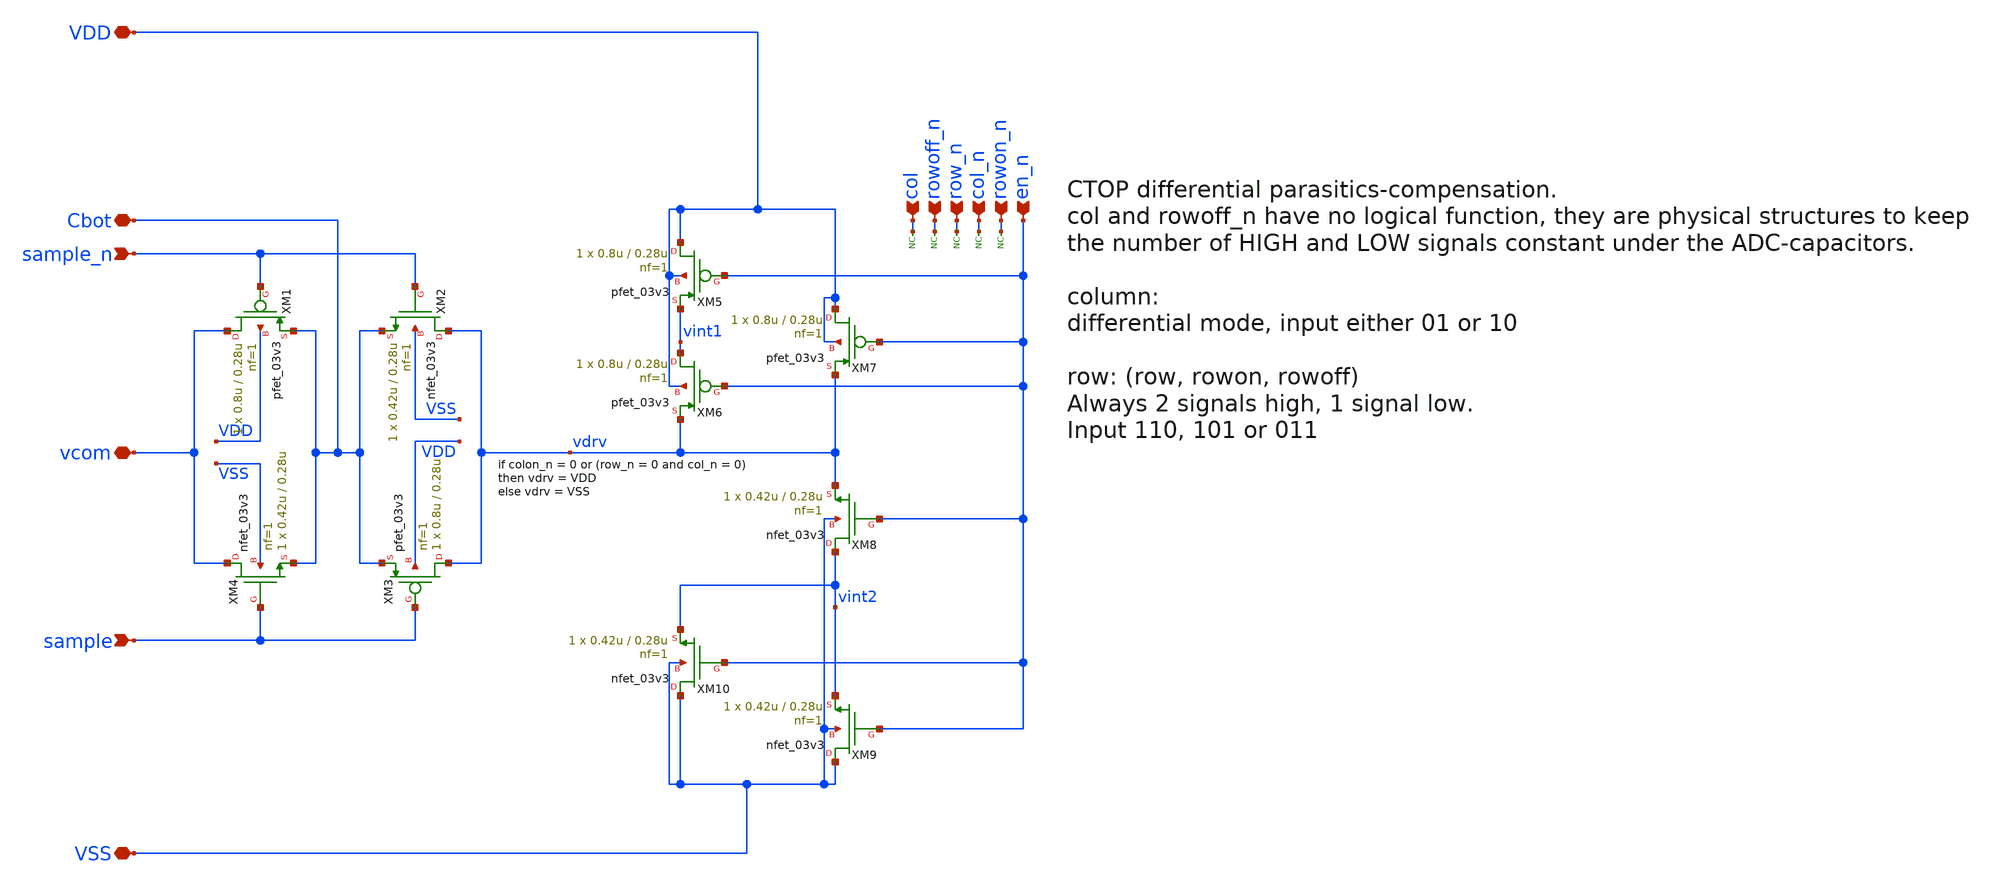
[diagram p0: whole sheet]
** sch_path: adc_sar_array_circuit_2.sch
**.subckt adc_sar_array_circuit_2 sample_n sample vcom row_n col_n rowon_n VDD VSS Cbot en_n
*+ rowoff_n col
*.ipin sample_n
*.ipin sample
*.iopin vcom
*.ipin row_n
*.ipin col_n
*.ipin rowon_n
*.iopin VDD
*.iopin VSS
*.iopin Cbot
*.ipin en_n
*.ipin rowoff_n
*.ipin col
* noconn row_n
* noconn col_n
* noconn rowon_n
* noconn rowoff_n
* noconn col
XM1 vcom sample_n Cbot VDD pfet_03v3 L=0.28u W=0.8u nf=1 ad='int((nf+1)/2) * W/nf * 0.18u' as='int((nf+2)/2) * W/nf * 0.18u'
+ pd='2*int((nf+1)/2) * (W/nf + 0.18u)' ps='2*int((nf+2)/2) * (W/nf + 0.18u)' nrd='0.18u / W' nrs='0.18u / W'
+ sa=0 sb=0 sd=0 m=1
XM2 vdrv sample_n Cbot VSS nfet_03v3 L=0.28u W=0.42u nf=1 ad='int((nf+1)/2) * W/nf * 0.18u' as='int((nf+2)/2) * W/nf * 0.18u'
+ pd='2*int((nf+1)/2) * (W/nf + 0.18u)' ps='2*int((nf+2)/2) * (W/nf + 0.18u)' nrd='0.18u / W' nrs='0.18u / W'
+ sa=0 sb=0 sd=0 m=1
XM3 vdrv sample Cbot VDD pfet_03v3 L=0.28u W=0.8u nf=1 ad='int((nf+1)/2) * W/nf * 0.18u' as='int((nf+2)/2) * W/nf * 0.18u'
+ pd='2*int((nf+1)/2) * (W/nf + 0.18u)' ps='2*int((nf+2)/2) * (W/nf + 0.18u)' nrd='0.18u / W' nrs='0.18u / W'
+ sa=0 sb=0 sd=0 m=1
XM4 vcom sample Cbot VSS nfet_03v3 L=0.28u W=0.42u nf=1 ad='int((nf+1)/2) * W/nf * 0.18u' as='int((nf+2)/2) * W/nf * 0.18u'
+ pd='2*int((nf+1)/2) * (W/nf + 0.18u)' ps='2*int((nf+2)/2) * (W/nf + 0.18u)' nrd='0.18u / W' nrs='0.18u / W'
+ sa=0 sb=0 sd=0 m=1
XM5 VDD en_n vint1 VDD pfet_03v3 L=0.28u W=0.8u nf=1 ad='int((nf+1)/2) * W/nf * 0.18u' as='int((nf+2)/2) * W/nf * 0.18u'
+ pd='2*int((nf+1)/2) * (W/nf + 0.18u)' ps='2*int((nf+2)/2) * (W/nf + 0.18u)' nrd='0.18u / W' nrs='0.18u / W'
+ sa=0 sb=0 sd=0 m=1
XM6 vint1 en_n vdrv VDD pfet_03v3 L=0.28u W=0.8u nf=1 ad='int((nf+1)/2) * W/nf * 0.18u' as='int((nf+2)/2) * W/nf * 0.18u'
+ pd='2*int((nf+1)/2) * (W/nf + 0.18u)' ps='2*int((nf+2)/2) * (W/nf + 0.18u)' nrd='0.18u / W' nrs='0.18u / W'
+ sa=0 sb=0 sd=0 m=1
XM7 VDD en_n vdrv VDD pfet_03v3 L=0.28u W=0.8u nf=1 ad='int((nf+1)/2) * W/nf * 0.18u' as='int((nf+2)/2) * W/nf * 0.18u'
+ pd='2*int((nf+1)/2) * (W/nf + 0.18u)' ps='2*int((nf+2)/2) * (W/nf + 0.18u)' nrd='0.18u / W' nrs='0.18u / W'
+ sa=0 sb=0 sd=0 m=1
XM8 vint2 en_n vdrv VSS nfet_03v3 L=0.28u W=0.42u nf=1 ad='int((nf+1)/2) * W/nf * 0.18u' as='int((nf+2)/2) * W/nf * 0.18u'
+ pd='2*int((nf+1)/2) * (W/nf + 0.18u)' ps='2*int((nf+2)/2) * (W/nf + 0.18u)' nrd='0.18u / W' nrs='0.18u / W'
+ sa=0 sb=0 sd=0 m=1
XM9 VSS en_n vint2 VSS nfet_03v3 L=0.28u W=0.42u nf=1 ad='int((nf+1)/2) * W/nf * 0.18u' as='int((nf+2)/2) * W/nf * 0.18u'
+ pd='2*int((nf+1)/2) * (W/nf + 0.18u)' ps='2*int((nf+2)/2) * (W/nf + 0.18u)' nrd='0.18u / W' nrs='0.18u / W'
+ sa=0 sb=0 sd=0 m=1
XM10 VSS en_n vint2 VSS nfet_03v3 L=0.28u W=0.42u nf=1 ad='int((nf+1)/2) * W/nf * 0.18u' as='int((nf+2)/2) * W/nf * 0.18u'
+ pd='2*int((nf+1)/2) * (W/nf + 0.18u)' ps='2*int((nf+2)/2) * (W/nf + 0.18u)' nrd='0.18u / W' nrs='0.18u / W'
+ sa=0 sb=0 sd=0 m=1
**.ends
.end
